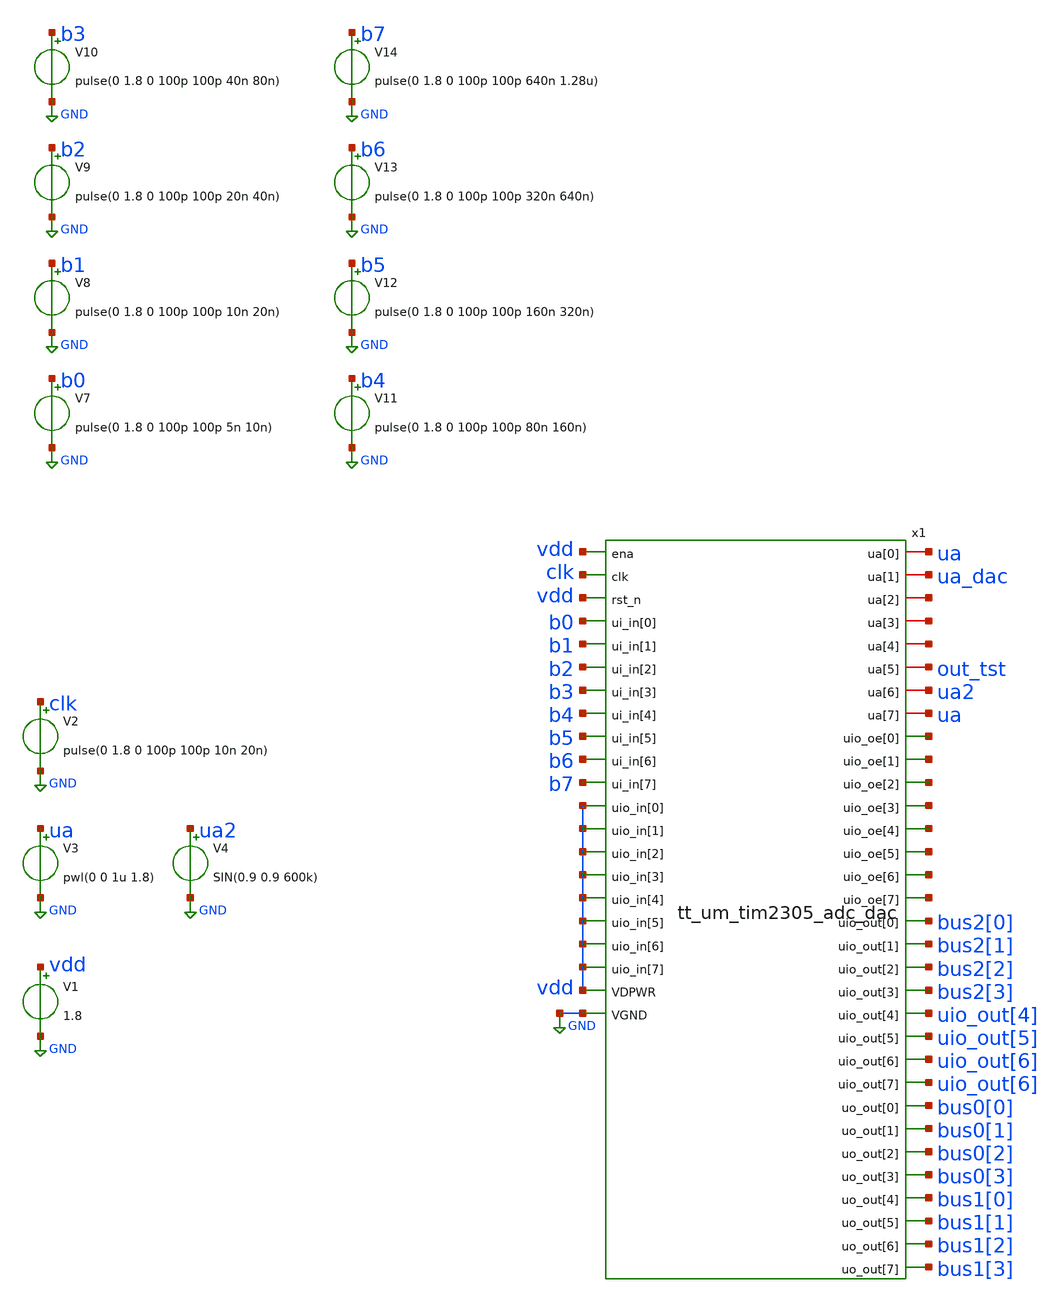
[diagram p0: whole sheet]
** sch_path: xschem/top_tb.sch
**.subckt top_tb
V1 vdd GND 1.8
V3 ua GND pwl(0 0 1u 1.8)
V2 clk GND pulse(0 1.8 0 100p 100p 10n 20n)
x1 ua ua_dac net1 net2 net3 out_tst ua2 vdd ua clk vdd net4 b0 net5 b1 net6 net7 b2 b3 net8 b4 net9
+ b5 net10 net11 b6 b7 bus2[0] vdd bus2[1] vdd bus2[2] vdd bus2[3] uio_out[4] vdd uio_out[5] vdd
+ uio_out[6] vdd vdd uio_out[6] vdd bus0[0] vdd bus0[1] GND bus0[2] bus0[3] bus1[0] bus1[1] bus1[2] bus1[3]
+ tt_um_tim2305_adc_dac
V4 ua2 GND SIN(0.9 0.9 600k)
V7 b0 GND pulse(0 1.8 0 100p 100p 5n 10n)
V8 b1 GND pulse(0 1.8 0 100p 100p 10n 20n)
V9 b2 GND pulse(0 1.8 0 100p 100p 20n 40n)
V10 b3 GND pulse(0 1.8 0 100p 100p 40n 80n)
V11 b4 GND pulse(0 1.8 0 100p 100p 80n 160n)
V12 b5 GND pulse(0 1.8 0 100p 100p 160n 320n)
V13 b6 GND pulse(0 1.8 0 100p 100p 320n 640n)
V14 b7 GND pulse(0 1.8 0 100p 100p 640n 1.28u)
**** begin user architecture code


.tran 100p 1u
.save all
.lib /home/ttuser/pdk/sky130A/libs.tech/ngspice/sky130.lib.spice tt
.include /home/ttuser/Documents/github_project/adc_dac2/mag/tt_um_tim2305_adc_dac.spice


**** end user architecture code
**.ends
.GLOBAL GND
.end
